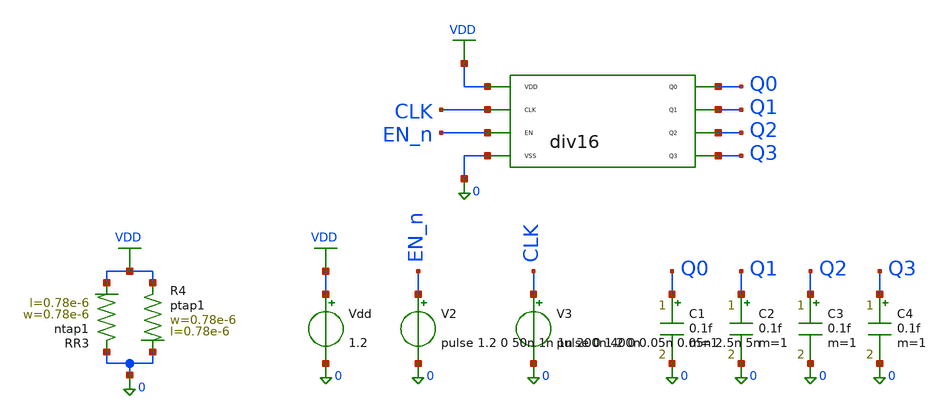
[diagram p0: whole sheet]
** sch_path: digital/div16/xschem/div16-tb.sch
**.subckt div16-tb
Vdd VDD 0 1.2
XR3 0 VDD ntap1 R=262.8 w=0.78e-6 l=0.78e-6
XR4 VDD 0 ptap1 R=262.8 w=0.78e-6 l=0.78e-6
V2 EN_n 0 pulse 1.2 0 50n 1n 1n 200n 400n
x1 0 VDD CLK EN_n Q0 Q1 Q2 Q3 div16
C1 Q0 0 0.1f m=1
C2 Q1 0 0.1f m=1
C3 Q2 0 0.1f m=1
C4 Q3 0 0.1f m=1
V3 CLK 0 pulse 0 1.2 0 0.05n 0.05n 2.5n 5n
**** begin user architecture code



** ngr_lib cornerMOSlv.lib mos_tt mos_ff mos_ss mos_tt_mismatch
** ngr_lib cornerRES.lib res_typ
** ngr_out f
** ngr_name div16-tb

.option rshunt=1e12
.option klu
*.param cpar=0
*.param lstarv=0.18u
.control
set rawfile = div16-tb.raw
tran 0.05n 300n

*meas tran tperiod
*  + TRIG v(ro_raw) VAL=0.6 RISE=2 TD=75n
*  + TARG v(ro_raw) VAL=0.6 RISE=3 TD=75n

write $rawfile clk en_n q0 q1 q2 q3
.endc






.lib cornerMOSlv.lib mos_tt
.lib cornerMOShv.lib mos_tt
.lib cornerRES.lib res_typ
.lib cornerDIO.lib dio_tt






.include sg13cmos5l_stdcell.spice
*.include digital/div16/div16.spice



**** end user architecture code
**.ends

* expanding   symbol:  digital/div16/xschem/div16.sym # of pins=8
** sym_path: digital/div16/xschem/div16.sym
.include digital/div16/div16.spice
.GLOBAL VDD
.end
